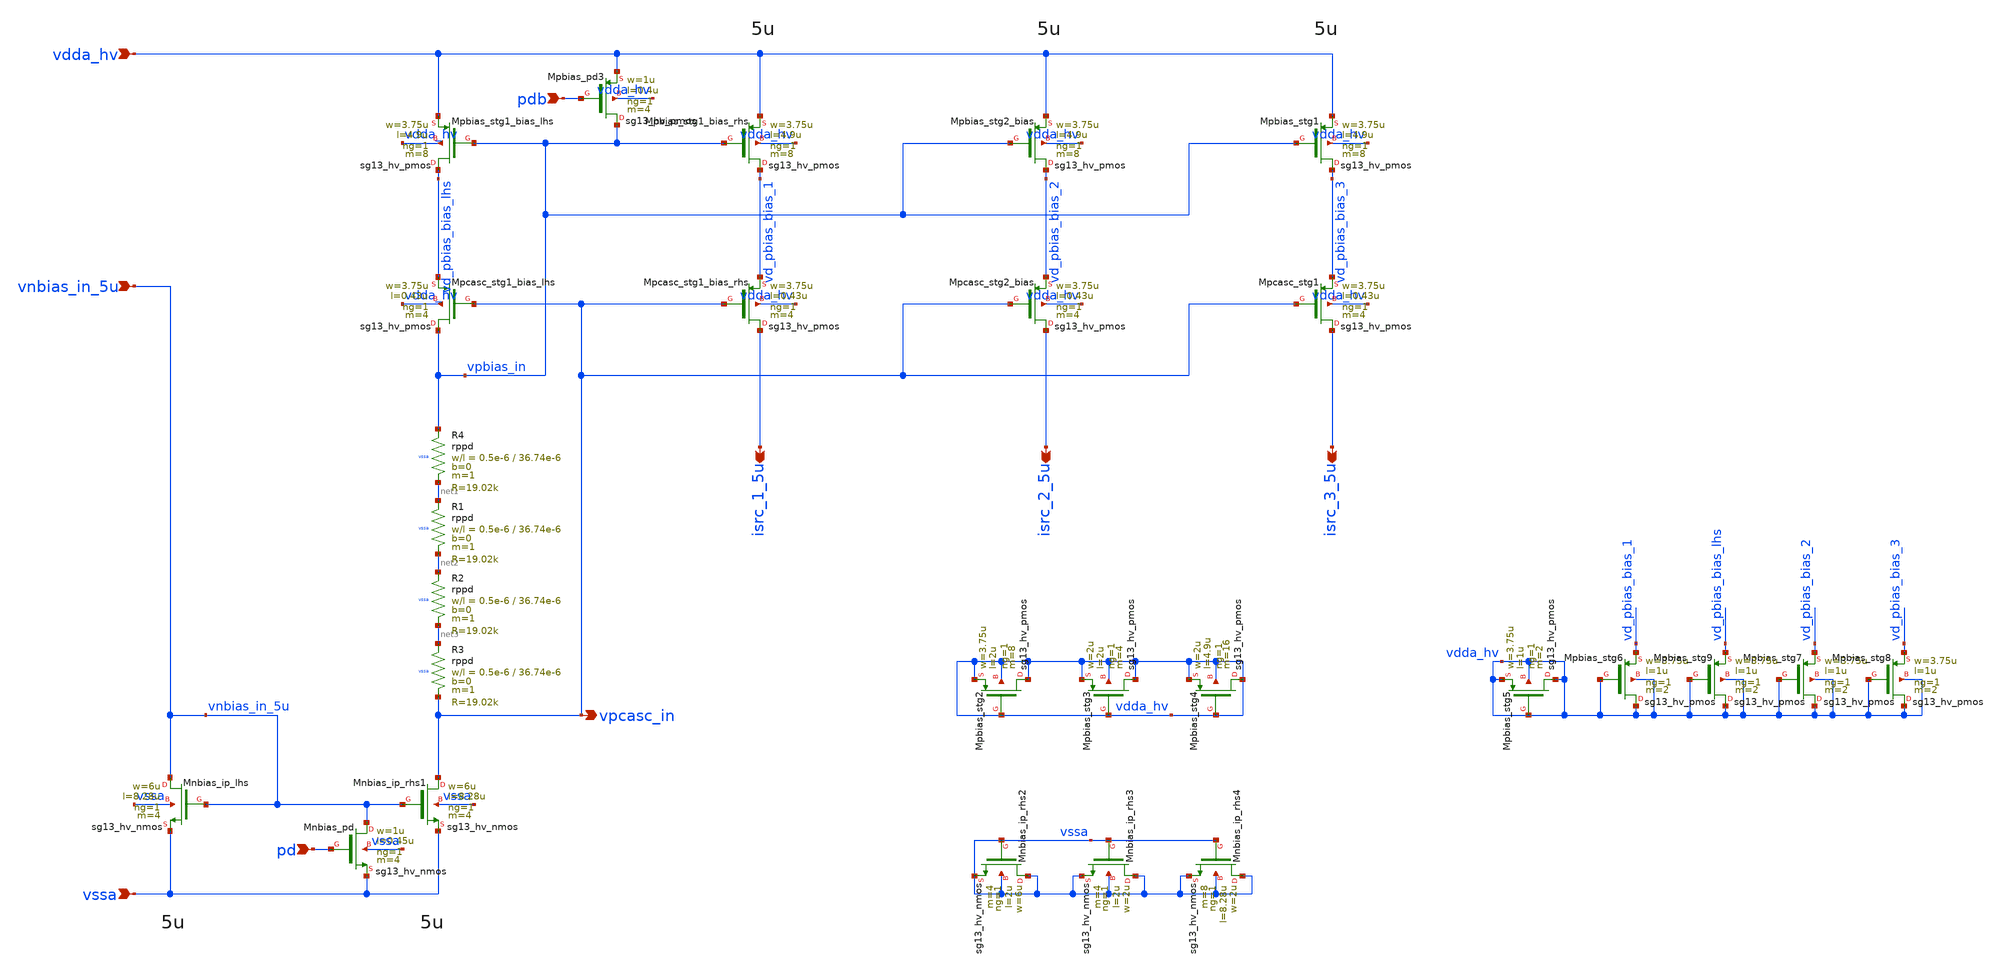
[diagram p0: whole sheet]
** sch_path: Schematics_Layout/sunrise_opamp_bias/sunrise_opamp_bias.sch
**.subckt sunrise_opamp_bias vdda_hv vssa vnbias_in_5u pd pdb vpcasc_in isrc_1_5u isrc_2_5u
*+ isrc_3_5u
*.ipin vdda_hv
*.ipin vssa
*.ipin vnbias_in_5u
*.ipin pd
*.ipin pdb
*.opin vpcasc_in
*.opin isrc_1_5u
*.opin isrc_2_5u
*.opin isrc_3_5u
XMnbias_ip_lhs vnbias_in_5u vnbias_in_5u vssa vssa sg13_hv_nmos w=6u l=8.28u ng=1 m=4 mm_ok=1
XMpcasc_stg1_bias_lhs vpbias_in vpcasc_in vd_pbias_bias_lhs vdda_hv sg13_hv_pmos w=3.75u l=0.43u
+ ng=1 m=4 mm_ok=1
XMpbias_stg1_bias_lhs vd_pbias_bias_lhs vpbias_in vdda_hv vdda_hv sg13_hv_pmos w=3.75u l=4.9u ng=1
+ m=8 mm_ok=1
XMpcasc_stg1_bias_rhs isrc_1_5u vpcasc_in vd_pbias_bias_1 vdda_hv sg13_hv_pmos w=3.75u l=0.43u ng=1
+ m=4 mm_ok=1
XMpbias_stg1_bias_rhs vd_pbias_bias_1 vpbias_in vdda_hv vdda_hv sg13_hv_pmos w=3.75u l=4.9u ng=1 m=8
+ mm_ok=1
XMpcasc_stg2_bias isrc_2_5u vpcasc_in vd_pbias_bias_2 vdda_hv sg13_hv_pmos w=3.75u l=0.43u ng=1 m=4
+ mm_ok=1
XMpbias_stg2_bias vd_pbias_bias_2 vpbias_in vdda_hv vdda_hv sg13_hv_pmos w=3.75u l=4.9u ng=1 m=8
+ mm_ok=1
XR4 vpbias_in net1 vssa rppd w=0.5e-6 l=36.74e-6 m=1 b=0 mm_ok=1
XMnbias_pd vnbias_in_5u pd vssa vssa sg13_hv_nmos w=1u l=0.45u ng=1 m=4 mm_ok=1
XMpbias_pd3 vpbias_in pdb vdda_hv vdda_hv sg13_hv_pmos w=1u l=0.4u ng=1 m=4 mm_ok=1
XMpcasc_stg1 isrc_3_5u vpcasc_in vd_pbias_bias_3 vdda_hv sg13_hv_pmos w=3.75u l=0.43u ng=1 m=4
+ mm_ok=1
XMpbias_stg1 vd_pbias_bias_3 vpbias_in vdda_hv vdda_hv sg13_hv_pmos w=3.75u l=4.9u ng=1 m=8 mm_ok=1
XMnbias_ip_rhs1 vpcasc_in vnbias_in_5u vssa vssa sg13_hv_nmos w=6u l=8.28u ng=1 m=4 mm_ok=1
XMnbias_ip_rhs2 vssa vssa vssa vssa sg13_hv_nmos w=6u l=2u ng=1 m=4 mm_ok=1
XMnbias_ip_rhs3 vssa vssa vssa vssa sg13_hv_nmos w=2u l=2u ng=1 m=4 mm_ok=1
XMnbias_ip_rhs4 vssa vssa vssa vssa sg13_hv_nmos w=2u l=8.28u ng=1 m=8 mm_ok=1
XMpbias_stg2 vdda_hv vdda_hv vdda_hv vdda_hv sg13_hv_pmos w=3.75u l=2u ng=1 m=8 mm_ok=1
XMpbias_stg3 vdda_hv vdda_hv vdda_hv vdda_hv sg13_hv_pmos w=2u l=2u ng=1 m=4 mm_ok=1
XMpbias_stg4 vdda_hv vdda_hv vdda_hv vdda_hv sg13_hv_pmos w=2u l=4.9u ng=1 m=16 mm_ok=1
XMpbias_stg5 vdda_hv vdda_hv vdda_hv vdda_hv sg13_hv_pmos w=3.75u l=1u ng=1 m=2 mm_ok=1
XMpbias_stg6 vdda_hv vdda_hv vd_pbias_bias_1 vdda_hv sg13_hv_pmos w=3.75u l=1u ng=1 m=2 mm_ok=1
XMpbias_stg7 vdda_hv vdda_hv vd_pbias_bias_2 vdda_hv sg13_hv_pmos w=3.75u l=1u ng=1 m=2 mm_ok=1
XMpbias_stg8 vdda_hv vdda_hv vd_pbias_bias_3 vdda_hv sg13_hv_pmos w=3.75u l=1u ng=1 m=2 mm_ok=1
XMpbias_stg9 vdda_hv vdda_hv vd_pbias_bias_lhs vdda_hv sg13_hv_pmos w=3.75u l=1u ng=1 m=2 mm_ok=1
XR1 net1 net2 vssa rppd w=0.5e-6 l=36.74e-6 m=1 b=0 mm_ok=1
XR2 net2 net3 vssa rppd w=0.5e-6 l=36.74e-6 m=1 b=0 mm_ok=1
XR3 net3 vpcasc_in vssa rppd w=0.5e-6 l=36.74e-6 m=1 b=0 mm_ok=1
**.ends
.end
